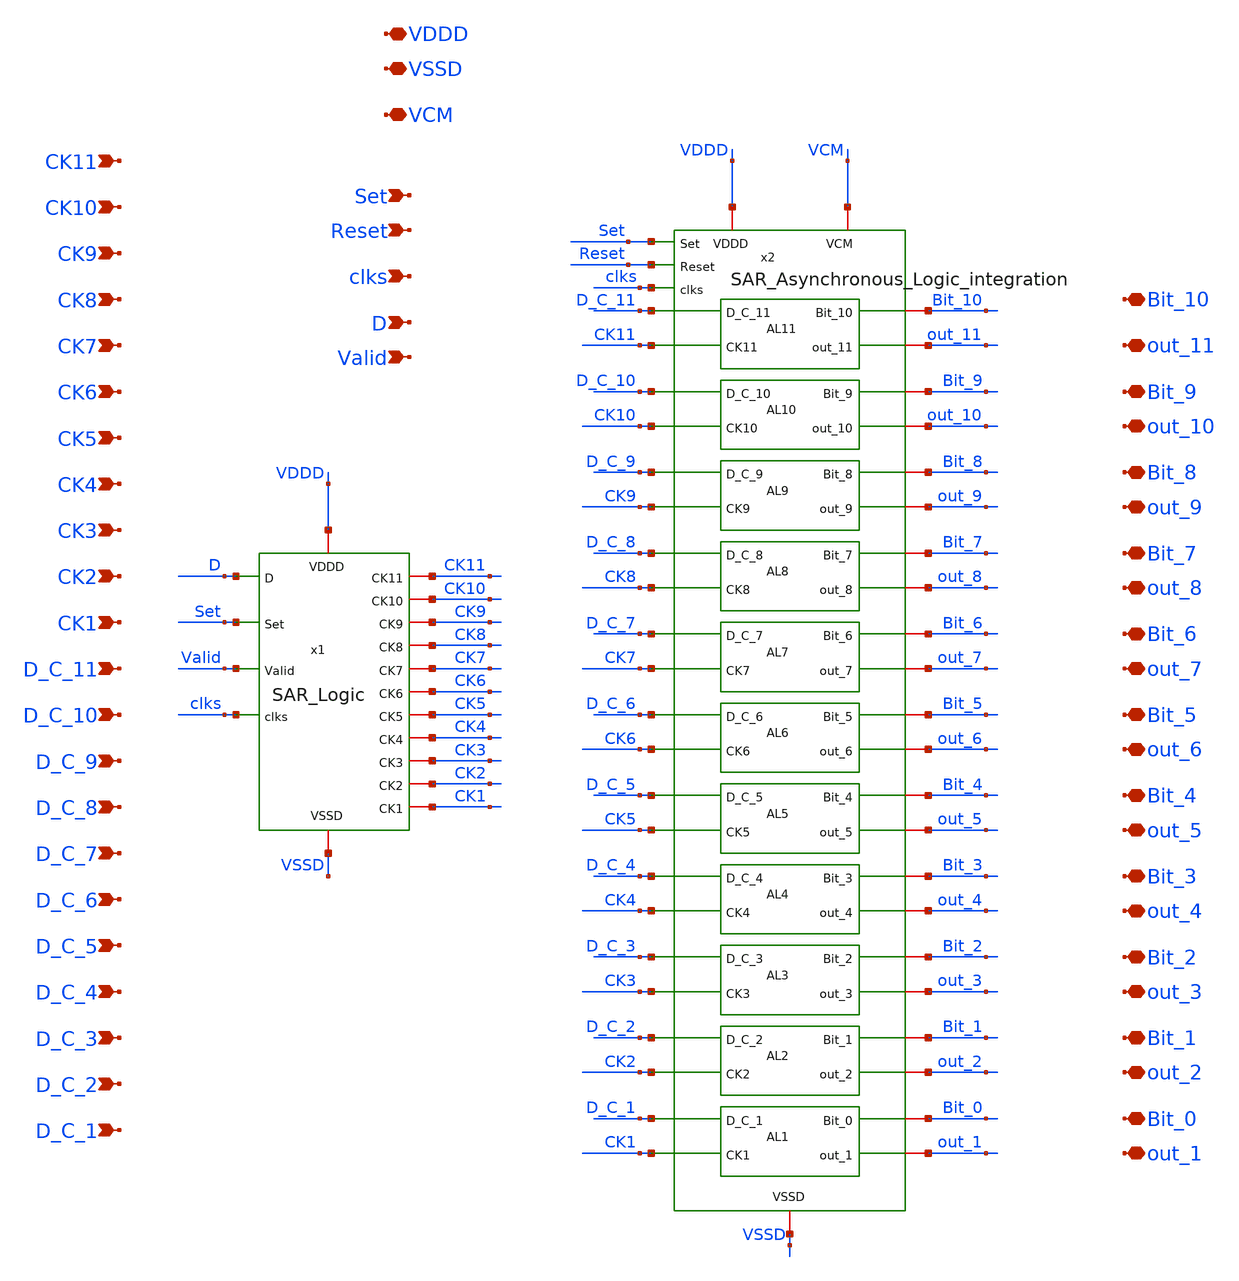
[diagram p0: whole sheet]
** sch_path: SAR_ADC/SAR_Asynchronous_top/SAR_Asynchronous_top.sch
**.subckt SAR_Asynchronous_top Bit_10 Bit_9 Bit_8 Bit_7 Bit_6 Bit_5 Bit_3 Bit_4 Bit_2 Bit_1 Bit_0
*+ out_11 out_10 out_9 out_8 out_7 out_6 out_5 out_4 out_3 out_2 out_1 VDDD VSSD Set Reset VCM clks D Valid
*+ D_C_11 D_C_10 D_C_9 D_C_8 D_C_7 D_C_6 D_C_5 D_C_4 D_C_3 D_C_2 D_C_1 CK11 CK10 CK9 CK8 CK7 CK6 CK5 CK4 CK3
*+ CK2 CK1
*.iopin Bit_10
*.iopin Bit_9
*.iopin Bit_8
*.iopin Bit_7
*.iopin Bit_6
*.iopin Bit_5
*.iopin Bit_3
*.iopin Bit_4
*.iopin Bit_2
*.iopin Bit_1
*.iopin Bit_0
*.iopin out_11
*.iopin out_10
*.iopin out_9
*.iopin out_8
*.iopin out_7
*.iopin out_6
*.iopin out_5
*.iopin out_4
*.iopin out_3
*.iopin out_2
*.iopin out_1
*.iopin VDDD
*.iopin VSSD
*.ipin Set
*.ipin Reset
*.iopin VCM
*.ipin clks
*.ipin D
*.ipin Valid
*.ipin D_C_11
*.ipin D_C_10
*.ipin D_C_9
*.ipin D_C_8
*.ipin D_C_7
*.ipin D_C_6
*.ipin D_C_5
*.ipin D_C_4
*.ipin D_C_3
*.ipin D_C_2
*.ipin D_C_1
*.ipin CK11
*.ipin CK10
*.ipin CK9
*.ipin CK8
*.ipin CK7
*.ipin CK6
*.ipin CK5
*.ipin CK4
*.ipin CK3
*.ipin CK2
*.ipin CK1
x1 CK11 VDDD CK1 CK6 VSSD CK10 CK5 CK9 CK4 clks CK8 CK3 Valid CK2 CK7 Set D SAR_Logic
x2 VDDD Bit_10 D_C_11 VSSD CK11 VCM out_11 Set Reset clks Bit_9 D_C_10 CK10 out_10 Bit_8 D_C_9 CK9
+ out_9 Bit_7 D_C_8 CK8 out_8 Bit_6 D_C_7 CK7 out_7 Bit_5 D_C_6 CK6 out_6 Bit_4 D_C_5 CK5 out_5 Bit_3 D_C_4
+ CK4 out_4 Bit_2 D_C_3 CK3 out_3 Bit_1 D_C_2 CK2 out_2 Bit_0 D_C_1 CK1 out_1
+ SAR_Asynchronous_Logic_integration
**.ends
.end
